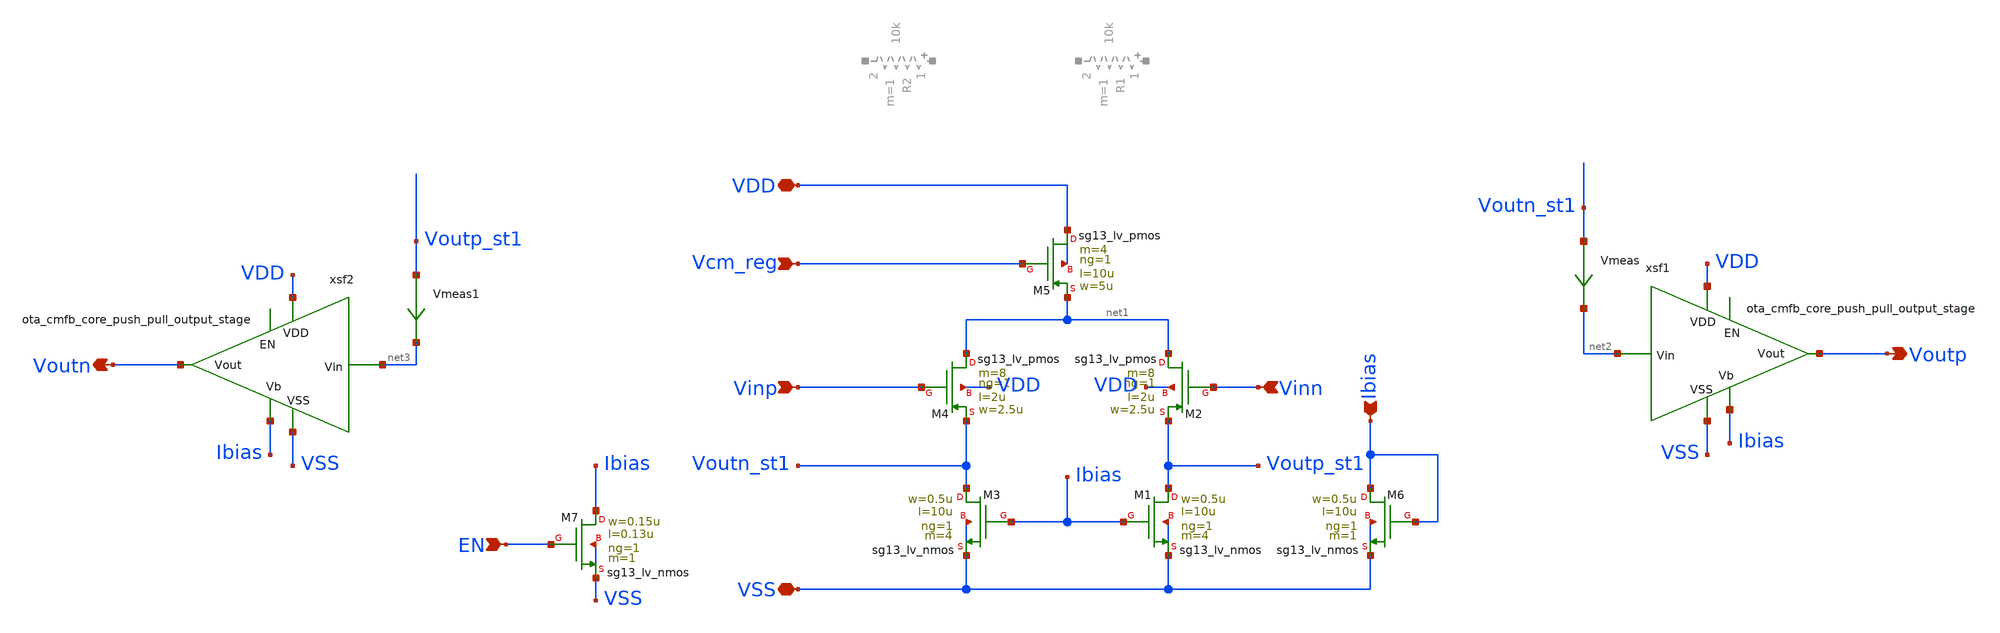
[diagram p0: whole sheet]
** sch_path: schema/ota_cmfb_core/ota_cmfb_core.sch
**.subckt ota_cmfb_core Voutn Voutp VDD VSS Vinp Ibias Vinn Vcm_reg EN
*.opin Voutn
*.opin Voutp
*.iopin VDD
*.iopin VSS
*.ipin Vinp
*.ipin Ibias
*.ipin Vinn
*.ipin Vcm_reg
*.ipin EN
XM1 Voutp_st1 Ibias VSS VSS sg13_lv_nmos w=0.5u l=10u ng=1 m=4 mm_ok=1
XM2 net1 Vinn Voutp_st1 VDD sg13_lv_pmos w=2.5u l=2u ng=1 m=8 mm_ok=1
XM3 Voutn_st1 Ibias VSS VSS sg13_lv_nmos w=0.5u l=10u ng=1 m=4 mm_ok=1
XM4 net1 Vinp Voutn_st1 VDD sg13_lv_pmos w=2.5u l=2u ng=1 m=8 mm_ok=1
XM5 VDD Vcm_reg net1 VDD sg13_lv_pmos w=5u l=10u ng=1 m=4 mm_ok=1
XM6 Ibias Ibias VSS VSS sg13_lv_nmos w=0.5u l=10u ng=1 m=1 mm_ok=1
XM7 Ibias EN VSS VSS sg13_lv_nmos w=0.15u l=0.13u ng=1 m=1 mm_ok=1
xsf1 VDD net2 Voutp Ibias VSS ota_cmfb_core_push_pull_output_stage
xsf2 VDD net3 Voutn Ibias VSS ota_cmfb_core_push_pull_output_stage
Vmeas Voutn_st1 net2 0
.save i(vmeas)
Vmeas1 Voutp_st1 net3 0
.save i(vmeas1)
**.ends

* expanding   symbol:
*+  /foss/designs/Chipalooza2/schema/ota_cmfb_core/ota_cmfb_core_push_pull_output_stage.sym # of pins=5
** sym_path: schema/ota_cmfb_core/ota_cmfb_core_push_pull_output_stage.sym
** sch_path: schema/ota_cmfb_core/ota_cmfb_core_push_pull_output_stage.sch
.subckt ota_cmfb_core_push_pull_output_stage VDD Vin Vout Vbias VSS
*.iopin VSS
*.iopin VDD
*.ipin Vbias
*.ipin Vin
*.opin Vout
XM1 Vout Vin_shifted VSS VSS sg13_lv_nmos w=2.5u l=0.5u ng=1 m=1 mm_ok=1
XM2 VDD Vin Vout VDD sg13_lv_pmos w=5u l=0.5u ng=1 m=1 mm_ok=1
XM5 VDD Vbiasp net2 VDD sg13_lv_pmos w=10u l=3u ng=1 m=1 mm_ok=1
XM6 net1 Vbiasn VSS VSS sg13_lv_nmos w=5u l=0.5u ng=1 m=1 mm_ok=1
XM4 Vin_shifted Vcasp2 Vin VDD sg13_lv_pmos w=5u l=3u ng=1 m=1 mm_ok=1
XM15 Vin_shifted Vcasn net1 VSS sg13_lv_nmos w=5u l=0.5u ng=1 m=1 mm_ok=1
XM16 net2 Vcasp Vin VDD sg13_lv_pmos w=10u l=3u ng=1 m=1 mm_ok=1
XM3 Vin Vcasn2 Vin_shifted VSS sg13_lv_nmos w=1.4u l=3u ng=1 m=1 mm_ok=1
XM8 VDD Vbiasp Vbiasp VDD sg13_lv_pmos w=10u l=3u ng=1 m=1 mm_ok=1
XM9 Vbiasp Vcasp Vcasp VDD sg13_lv_pmos w=10u l=3u ng=1 m=1 mm_ok=1
XM13 Vcasp Vcasp2 Vcasp2 VDD sg13_lv_pmos w=5u l=3u ng=1 m=2 mm_ok=1
XM10 VDD Vbiasp Vcasn2 VDD sg13_lv_pmos w=10u l=3u ng=1 m=1 mm_ok=1
XM11 Vcasn2 Vcasn2 Vcasn VSS sg13_lv_nmos w=1.4u l=3u ng=1 m=2 mm_ok=1
XM12 Vcasn Vcasn Vbiasn VSS sg13_lv_nmos w=5u l=0.5u ng=1 m=1 mm_ok=1
XM14 Vbiasn Vbiasn VSS VSS sg13_lv_nmos w=5u l=0.5u ng=1 m=1 mm_ok=1
XM7 Vcasp2 Vbias VSS VSS sg13_lv_nmos w=2u l=1u ng=1 m=2 mm_ok=1
XR1 net3 Vout sub! rhigh w=0.5e-6 l=1e-6 m=1 b=0 mm_ok=1
XR2 net4 Vout sub! rhigh w=0.5e-6 l=1e-6*2 m=1 b=0 mm_ok=1
XC1 net3 Vin sg13_moscap_p w=5.0u l=5.0u m=3 mm_ok=1
XC2 net4 Vin_shifted sg13_moscap_p w=5.0u l=5.0u m=3 mm_ok=1
.ends

.end
